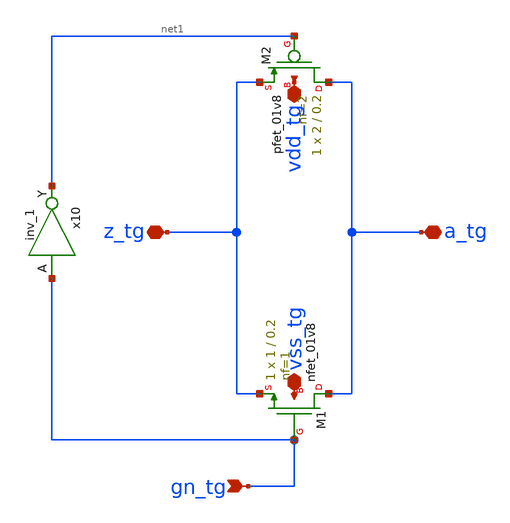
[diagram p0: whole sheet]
** sch_path: tg.sch
**.subckt tg a_tg z_tg gn_tg vss_tg vdd_tg
*.iopin a_tg
*.iopin z_tg
*.ipin gn_tg
*.iopin vss_tg
*.iopin vdd_tg
XM1 a_tg gn_tg z_tg vss_tg sky130_fd_pr__nfet_01v8 L=0.2 W=1 nf=1 ad='int((nf+1)/2) * W/nf * 0.29' as='int((nf+2)/2) * W/nf * 0.29'
+ pd='2*int((nf+1)/2) * (W/nf + 0.29)' ps='2*int((nf+2)/2) * (W/nf + 0.29)' nrd='0.29 / W' nrs='0.29 / W'
+ sa=0 sb=0 sd=0 mult=1 m=1
XM2 a_tg net1 z_tg vdd_tg sky130_fd_pr__pfet_01v8 L=0.2 W=2 nf=2 ad='int((nf+1)/2) * W/nf * 0.29' as='int((nf+2)/2) * W/nf * 0.29'
+ pd='2*int((nf+1)/2) * (W/nf + 0.29)' ps='2*int((nf+2)/2) * (W/nf + 0.29)' nrd='0.29 / W' nrs='0.29 / W'
+ sa=0 sb=0 sd=0 mult=1 m=1
x10 gn_tg vss_tg vss_tg vdd_tg vdd_tg net1 sky130_fd_sc_hd__inv_1
**.ends
.end
